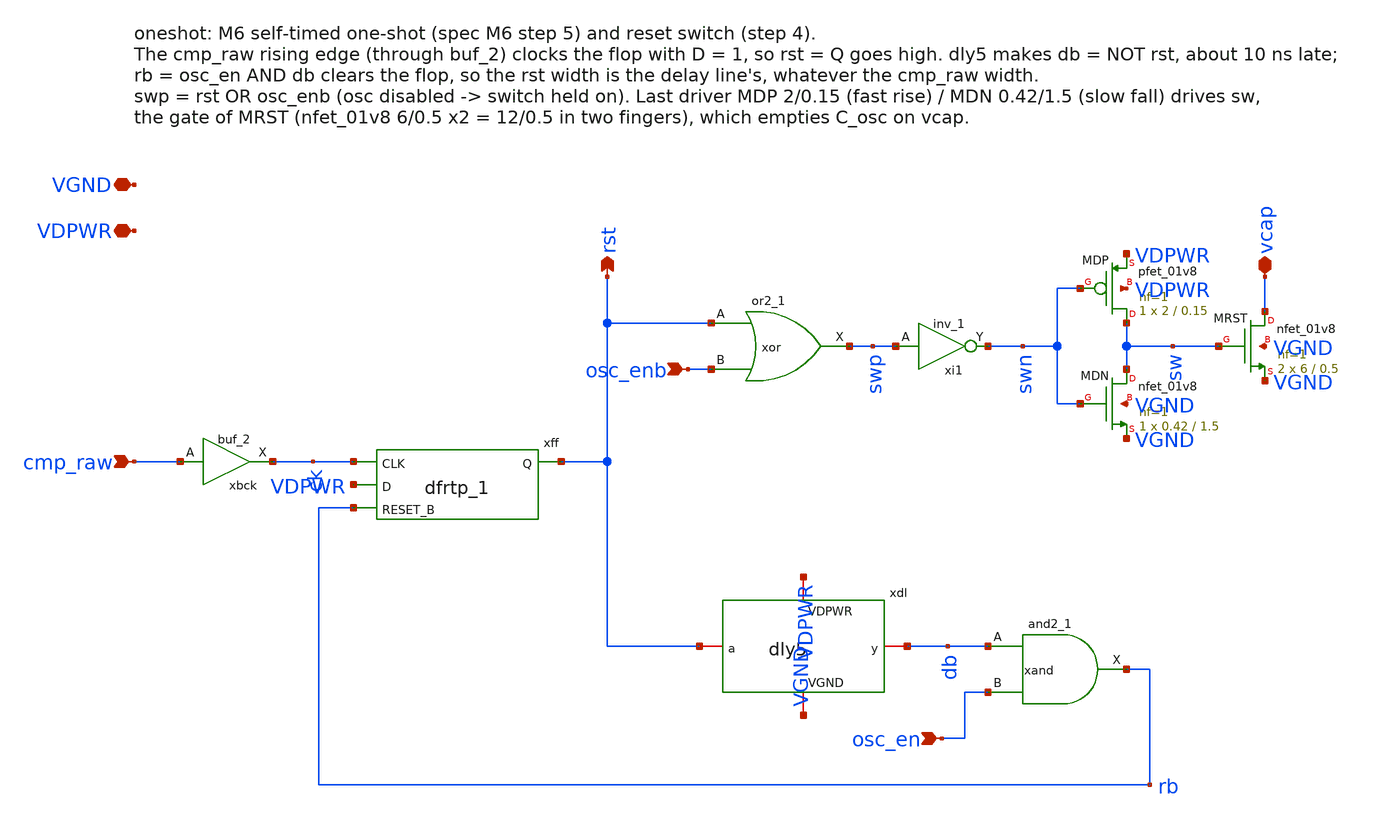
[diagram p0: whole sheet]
** sch_path: xschem/oneshot.sch
**.subckt oneshot cmp_raw osc_enb osc_en vcap rst VDPWR VGND
*.ipin cmp_raw
*.ipin osc_enb
*.ipin osc_en
*.iopin vcap
*.opin rst
*.iopin VDPWR
*.iopin VGND
xbck cmp_raw VGND VGND VDPWR VDPWR ck sky130_fd_sc_hd__buf_2
xff ck VDPWR rb VGND VGND VDPWR VDPWR rst sky130_fd_sc_hd__dfrtp_1
xor rst osc_enb VGND VGND VDPWR VDPWR swp sky130_fd_sc_hd__or2_1
xi1 swp VGND VGND VDPWR VDPWR swn sky130_fd_sc_hd__inv_1
xand db osc_en VGND VGND VDPWR VDPWR rb sky130_fd_sc_hd__and2_1
xdl rst db VDPWR VGND dly5
XMDP sw swn VDPWR VDPWR sky130_fd_pr__pfet_01v8 L=0.15 W=2 nf=1 ad='int((1 + 1)/2) * 2 / 1 * 0.29' as='int((1 + 2)/2) * 2 / 1 * 0.29'
+ pd='2*int((1 + 1)/2) * (2 / 1 + 0.29)' ps='2*int((1 + 2)/2) * (2 / 1 + 0.29)' nrd='0.29 / 2 ' nrs='0.29 / 2 '
+ sa=0 sb=0 sd=0 mult=1 m=1
XMDN sw swn VGND VGND sky130_fd_pr__nfet_01v8 L=1.5 W=0.42 nf=1 ad='int((1 + 1)/2) * 0.42 / 1 * 0.29'
+ as='int((1 + 2)/2) * 0.42 / 1 * 0.29' pd='2*int((1 + 1)/2) * (0.42 / 1 + 0.29)' ps='2*int((1 + 2)/2) * (0.42 / 1 + 0.29)'
+ nrd='0.29 / 0.42 ' nrs='0.29 / 0.42 ' sa=0 sb=0 sd=0 mult=1 m=1
XMRST vcap sw VGND VGND sky130_fd_pr__nfet_01v8 L=0.5 W=6 nf=1 ad='int((1 + 1)/2) * 6 / 1 * 0.29' as='int((1 + 2)/2) * 6 / 1 * 0.29'
+ pd='2*int((1 + 1)/2) * (6 / 1 + 0.29)' ps='2*int((1 + 2)/2) * (6 / 1 + 0.29)' nrd='0.29 / 6 ' nrs='0.29 / 6 '
+ sa=0 sb=0 sd=0 mult=2 m=2
**.ends

* expanding   symbol:  dly5.sym # of pins=4
** sym_path: xschem/dly5.sym
** sch_path: xschem/dly5.sch
.subckt dly5 a y VDPWR VGND
*.iopin VDPWR
*.iopin VGND
*.ipin a
*.opin y
XMP1 d1 a VDPWR VDPWR sky130_fd_pr__pfet_01v8 L=2.3 W=1 nf=1 ad='int((1 + 1)/2) * 1 / 1 * 0.29' as='int((1 + 2)/2) * 1 / 1 * 0.29'
+ pd='2*int((1 + 1)/2) * (1 / 1 + 0.29)' ps='2*int((1 + 2)/2) * (1 / 1 + 0.29)' nrd='0.29 / 1 ' nrs='0.29 / 1 '
+ sa=0 sb=0 sd=0 mult=1 m=1
XMN1 d1 a VGND VGND sky130_fd_pr__nfet_01v8 L=2.3 W=0.42 nf=1 ad='int((1 + 1)/2) * 0.42 / 1 * 0.29' as='int((1 + 2)/2) * 0.42 / 1 * 0.29'
+ pd='2*int((1 + 1)/2) * (0.42 / 1 + 0.29)' ps='2*int((1 + 2)/2) * (0.42 / 1 + 0.29)' nrd='0.29 / 0.42 '
+ nrs='0.29 / 0.42 ' sa=0 sb=0 sd=0 mult=1 m=1
XMP2 d2 d1 VDPWR VDPWR sky130_fd_pr__pfet_01v8 L=2.3 W=1 nf=1 ad='int((1 + 1)/2) * 1 / 1 * 0.29' as='int((1 + 2)/2) * 1 / 1 * 0.29'
+ pd='2*int((1 + 1)/2) * (1 / 1 + 0.29)' ps='2*int((1 + 2)/2) * (1 / 1 + 0.29)' nrd='0.29 / 1 ' nrs='0.29 / 1 '
+ sa=0 sb=0 sd=0 mult=1 m=1
XMN2 d2 d1 VGND VGND sky130_fd_pr__nfet_01v8 L=2.3 W=0.42 nf=1 ad='int((1 + 1)/2) * 0.42 / 1 * 0.29'
+ as='int((1 + 2)/2) * 0.42 / 1 * 0.29' pd='2*int((1 + 1)/2) * (0.42 / 1 + 0.29)' ps='2*int((1 + 2)/2) * (0.42 / 1 + 0.29)'
+ nrd='0.29 / 0.42 ' nrs='0.29 / 0.42 ' sa=0 sb=0 sd=0 mult=1 m=1
XMP3 d3 d2 VDPWR VDPWR sky130_fd_pr__pfet_01v8 L=2.3 W=1 nf=1 ad='int((1 + 1)/2) * 1 / 1 * 0.29' as='int((1 + 2)/2) * 1 / 1 * 0.29'
+ pd='2*int((1 + 1)/2) * (1 / 1 + 0.29)' ps='2*int((1 + 2)/2) * (1 / 1 + 0.29)' nrd='0.29 / 1 ' nrs='0.29 / 1 '
+ sa=0 sb=0 sd=0 mult=1 m=1
XMN3 d3 d2 VGND VGND sky130_fd_pr__nfet_01v8 L=2.3 W=0.42 nf=1 ad='int((1 + 1)/2) * 0.42 / 1 * 0.29'
+ as='int((1 + 2)/2) * 0.42 / 1 * 0.29' pd='2*int((1 + 1)/2) * (0.42 / 1 + 0.29)' ps='2*int((1 + 2)/2) * (0.42 / 1 + 0.29)'
+ nrd='0.29 / 0.42 ' nrs='0.29 / 0.42 ' sa=0 sb=0 sd=0 mult=1 m=1
XMP4 d4 d3 VDPWR VDPWR sky130_fd_pr__pfet_01v8 L=2.3 W=1 nf=1 ad='int((1 + 1)/2) * 1 / 1 * 0.29' as='int((1 + 2)/2) * 1 / 1 * 0.29'
+ pd='2*int((1 + 1)/2) * (1 / 1 + 0.29)' ps='2*int((1 + 2)/2) * (1 / 1 + 0.29)' nrd='0.29 / 1 ' nrs='0.29 / 1 '
+ sa=0 sb=0 sd=0 mult=1 m=1
XMN4 d4 d3 VGND VGND sky130_fd_pr__nfet_01v8 L=2.3 W=0.42 nf=1 ad='int((1 + 1)/2) * 0.42 / 1 * 0.29'
+ as='int((1 + 2)/2) * 0.42 / 1 * 0.29' pd='2*int((1 + 1)/2) * (0.42 / 1 + 0.29)' ps='2*int((1 + 2)/2) * (0.42 / 1 + 0.29)'
+ nrd='0.29 / 0.42 ' nrs='0.29 / 0.42 ' sa=0 sb=0 sd=0 mult=1 m=1
XMP5 y d4 VDPWR VDPWR sky130_fd_pr__pfet_01v8 L=2.3 W=1 nf=1 ad='int((1 + 1)/2) * 1 / 1 * 0.29' as='int((1 + 2)/2) * 1 / 1 * 0.29'
+ pd='2*int((1 + 1)/2) * (1 / 1 + 0.29)' ps='2*int((1 + 2)/2) * (1 / 1 + 0.29)' nrd='0.29 / 1 ' nrs='0.29 / 1 '
+ sa=0 sb=0 sd=0 mult=1 m=1
XMN5 y d4 VGND VGND sky130_fd_pr__nfet_01v8 L=2.3 W=0.42 nf=1 ad='int((1 + 1)/2) * 0.42 / 1 * 0.29' as='int((1 + 2)/2) * 0.42 / 1 * 0.29'
+ pd='2*int((1 + 1)/2) * (0.42 / 1 + 0.29)' ps='2*int((1 + 2)/2) * (0.42 / 1 + 0.29)' nrd='0.29 / 0.42 '
+ nrs='0.29 / 0.42 ' sa=0 sb=0 sd=0 mult=1 m=1
.ends

.end
